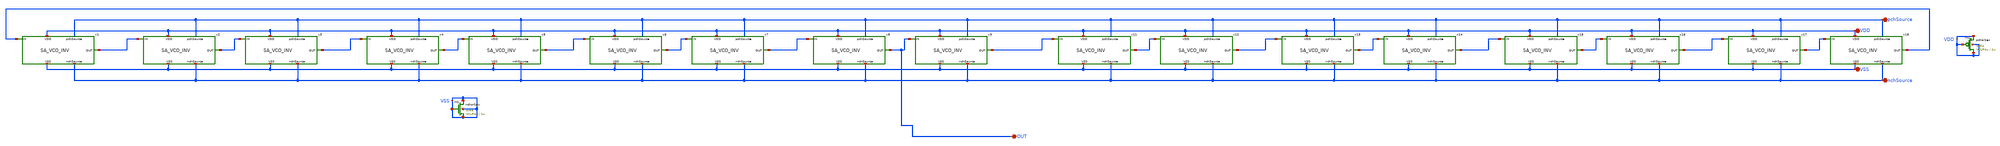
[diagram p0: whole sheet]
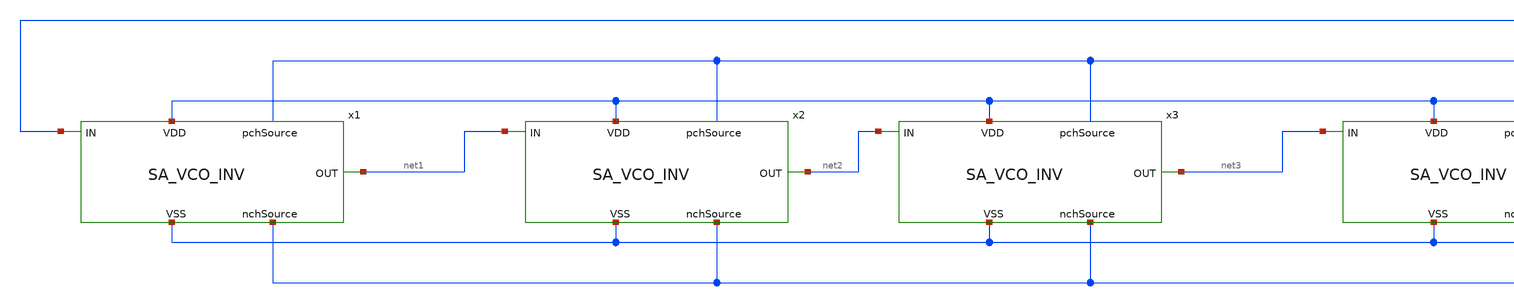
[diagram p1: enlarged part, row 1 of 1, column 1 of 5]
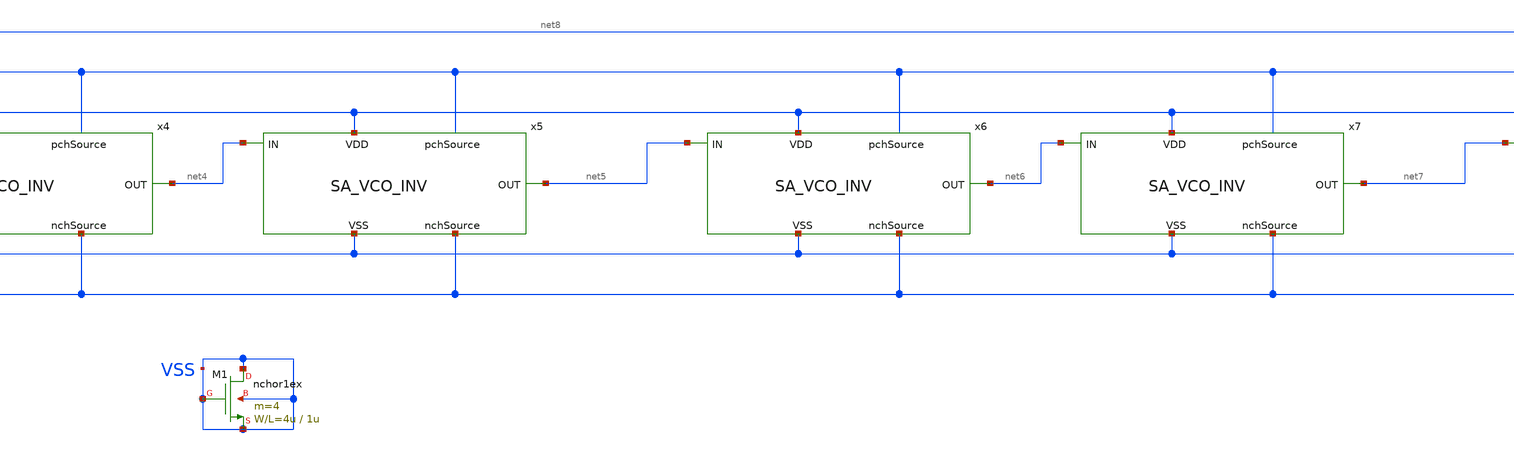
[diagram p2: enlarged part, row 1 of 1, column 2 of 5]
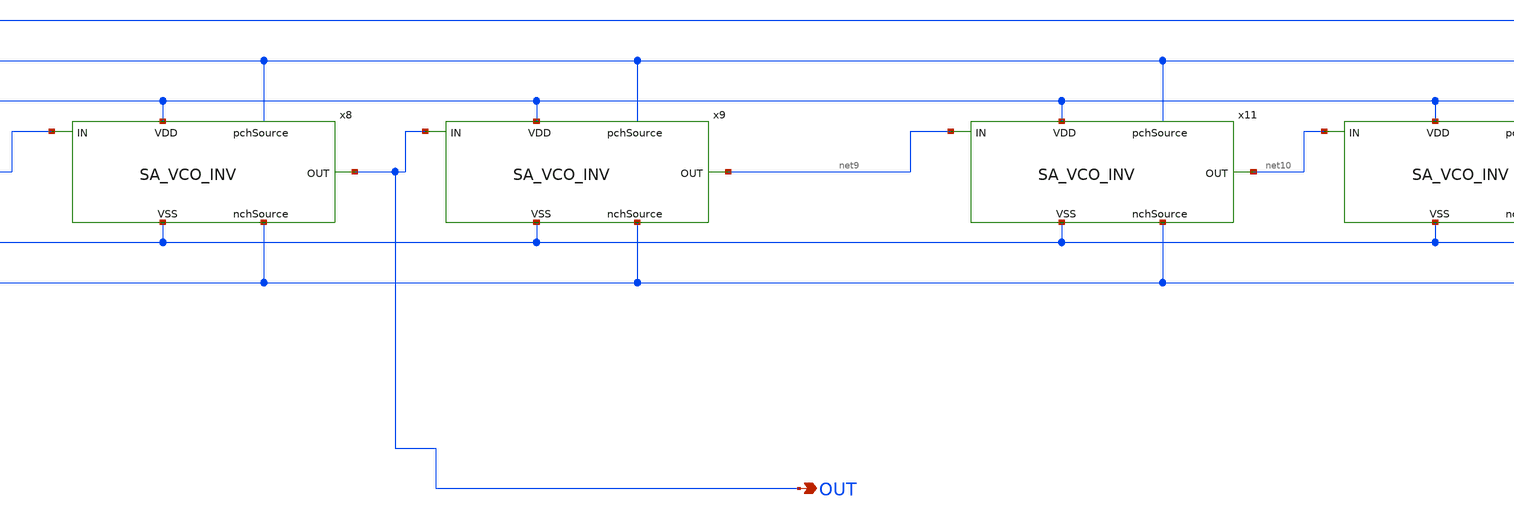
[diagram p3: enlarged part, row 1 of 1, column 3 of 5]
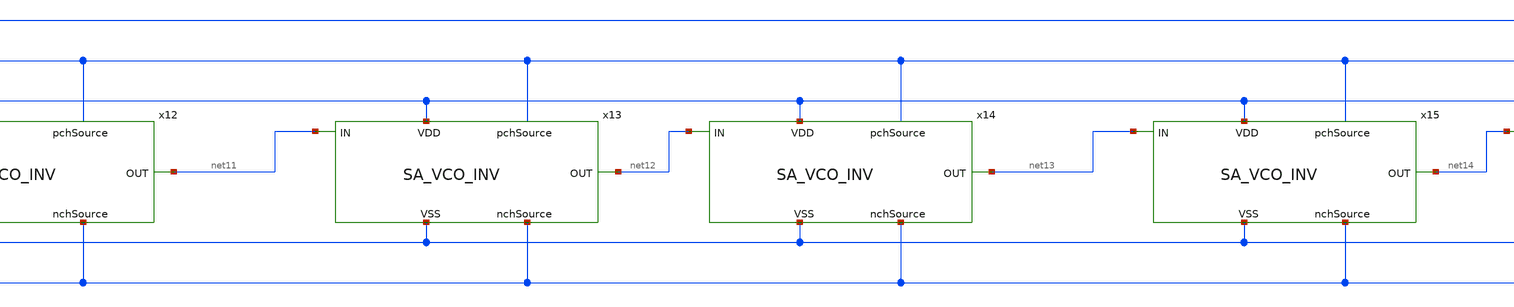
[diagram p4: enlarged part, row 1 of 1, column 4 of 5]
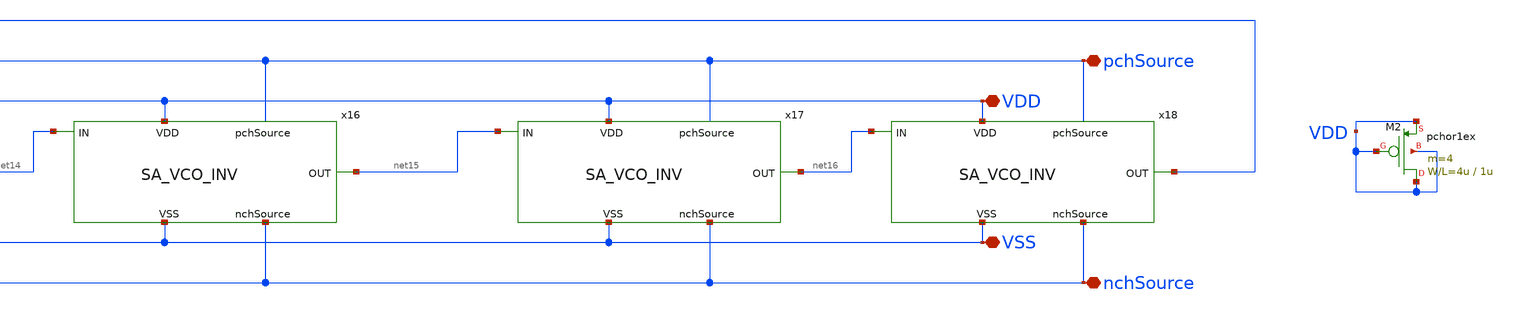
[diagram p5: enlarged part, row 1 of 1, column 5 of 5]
** sch_path: design/xschem/VCO/RO_9.sch
**.subckt RO_9 pchSource VDD VSS nchSource OUT
*.iopin pchSource
*.iopin VDD
*.iopin VSS
*.iopin nchSource
*.opin OUT
x2 VDD net1 net2 VSS nchSource SA_VCO_INV
x3 VDD net2 net3 VSS nchSource SA_VCO_INV
x4 VDD net3 net4 VSS nchSource SA_VCO_INV
x5 VDD net4 net5 VSS nchSource SA_VCO_INV
x6 VDD net5 net6 VSS nchSource SA_VCO_INV
x7 VDD net6 net7 VSS nchSource SA_VCO_INV
x8 VDD net7 OUT VSS nchSource SA_VCO_INV
x9 VDD OUT net9 VSS nchSource SA_VCO_INV
x1 VDD net8 net1 VSS nchSource SA_VCO_INV
x11 VDD net9 net10 VSS nchSource SA_VCO_INV
x12 VDD net10 net11 VSS nchSource SA_VCO_INV
x13 VDD net11 net12 VSS nchSource SA_VCO_INV
x14 VDD net12 net13 VSS nchSource SA_VCO_INV
x15 VDD net13 net14 VSS nchSource SA_VCO_INV
x16 VDD net14 net15 VSS nchSource SA_VCO_INV
x17 VDD net15 net16 VSS nchSource SA_VCO_INV
x18 VDD net16 net8 VSS nchSource SA_VCO_INV
M1 VSS VSS VSS VSS nchor1ex L=1u W=4u m=4
M2 VDD VDD VDD VDD pchor1ex L=1u W=4u m=4
**.ends

* expanding   symbol:  VCO/SA_VCO_INV.sym # of pins=5
** sym_path: design/xschem/VCO/SA_VCO_INV.sym
** sch_path: design/xschem/VCO/SA_VCO_INV.sch
.subckt SA_VCO_INV VDD IN OUT VSS nchSource
*.iopin nchSource
*.ipin IN
*.opin OUT
*.iopin VDD
*.iopin VSS
M1 VSS OUT VSS VSS nchor1ex L=3u W=6u m=1
M2 OUT IN VDD VDD pchor1ex L=1u W=4u m=4
M3 OUT IN nchSource VSS nchor1ex L=1u W=4u m=2
.ends

.end
